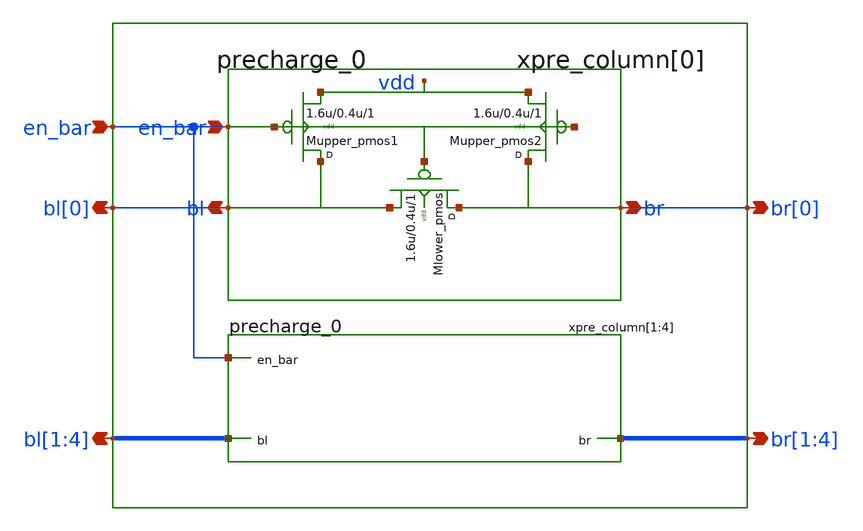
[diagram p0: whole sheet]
** sch_path: sram_4_16_scn4m/precharge_array.sch
**.subckt precharge_array bl[0] br[0] en_bar bl[1],bl[2],bl[3],bl[4] br[1],br[2],br[3],br[4]
*.opin bl[0]
*.opin br[0]
*.ipin en_bar
*.opin bl[1],bl[2],bl[3],bl[4]
*.opin br[1],br[2],br[3],br[4]
xpre_column[0] bl[0] br[0] en_bar vdd precharge_0
xpre_column[1] bl[1] br[1] en_bar vdd precharge_0
xpre_column[2] bl[2] br[2] en_bar vdd precharge_0
xpre_column[3] bl[3] br[3] en_bar vdd precharge_0
xpre_column[4] bl[4] br[4] en_bar vdd precharge_0
**.ends

* expanding   symbol:  precharge_0.sch # of pins=3
** sym_path: sram_4_16_scn4m/precharge_0.sch
** sch_path: sram_4_16_scn4m/precharge_0.sch
.subckt precharge_0 bl br en_bar vdd
*.opin bl
*.opin br
*.ipin en_bar
Mupper_pmos1 bl en_bar vdd vdd p w=1.6u l=0.4u m=1
Mupper_pmos2 br en_bar vdd vdd p w=1.6u l=0.4u m=1
Mlower_pmos br en_bar bl vdd p w=1.6u l=0.4u m=1
.ends

.end
